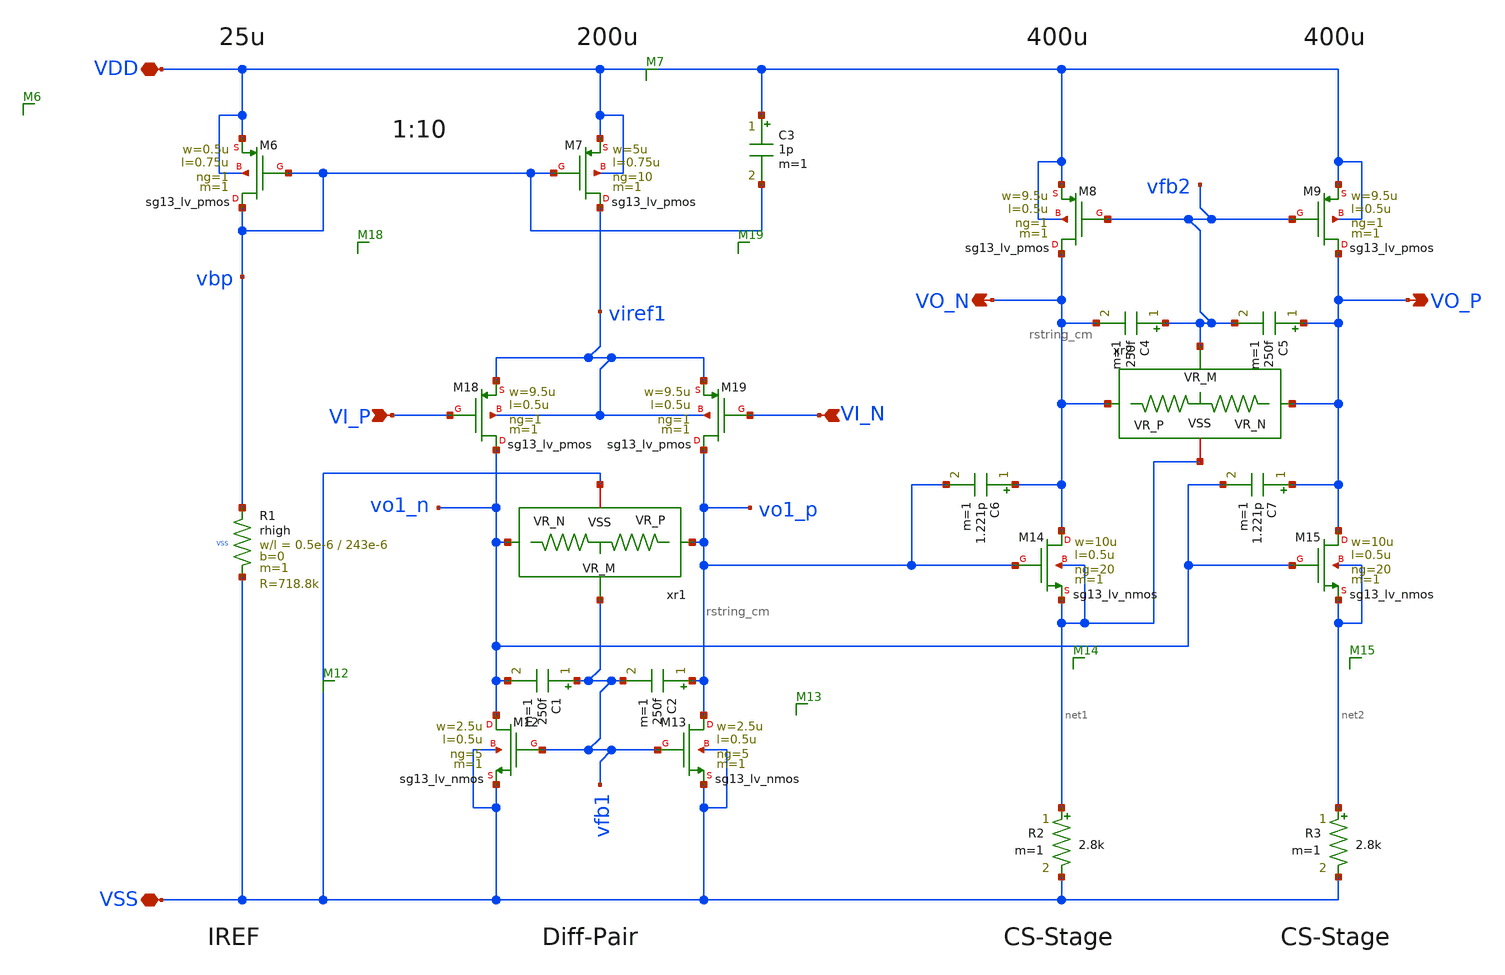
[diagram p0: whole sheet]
** sch_path: macros/filter_cmos5l/schematic/xschem/amp_no_enable.sch
**.subckt amp_no_enable VSS VDD VI_P VI_N VO_P VO_N
*.iopin VSS
*.iopin VDD
*.ipin VI_P
*.ipin VI_N
*.opin VO_P
*.opin VO_N
xr1 vfb1 vo1_n vo1_p VSS rstring_cm
xr2 vfb2 VO_P VO_N net1 rstring_cm
XM6 vbp vbp VDD VDD sg13_lv_pmos w=0.5u l=0.75u ng=1 m=1 mm_ok=1
XM7 viref1 vbp VDD VDD sg13_lv_pmos w=5u l=0.75u ng=10 m=1 mm_ok=1
XM8 VO_N vfb2 VDD VDD sg13_lv_pmos w=9.5u l=0.5u ng=1 m=1 mm_ok=1
XM9 VO_P vfb2 VDD VDD sg13_lv_pmos w=9.5u l=0.5u ng=1 m=1 mm_ok=1
XM12 vo1_n vfb1 VSS VSS sg13_lv_nmos w=2.5u l=0.5u ng=5 m=1 mm_ok=1
XM13 vo1_p vfb1 VSS VSS sg13_lv_nmos w=2.5u l=0.5u ng=5 m=1 mm_ok=1
XM14 VO_N vo1_p net1 net1 sg13_lv_nmos w=10u l=0.5u ng=20 m=1 mm_ok=1
XM15 VO_P vo1_n net2 net2 sg13_lv_nmos w=10u l=0.5u ng=20 m=1 mm_ok=1
XM18 vo1_n VI_P viref1 viref1 sg13_lv_pmos w=9.5u l=0.5u ng=1 m=1 mm_ok=1
XM19 vo1_p VI_N viref1 viref1 sg13_lv_pmos w=9.5u l=0.5u ng=1 m=1 mm_ok=1
XR1 vbp VSS VSS rhigh w=0.5e-6 l=243e-6 m=1 b=0 mm_ok=1
C6 VO_N vo1_p 1.221p m=1
C1 vfb1 vo1_n 250f m=1
C7 VO_P vo1_n 1.221p m=1
C3 VDD vbp 1p m=1
C2 vo1_p vfb1 250f m=1
C4 vfb2 VO_N 250f m=1
C5 VO_P vfb2 250f m=1
R2 net1 VSS 2.8k m=1
R3 net2 VSS 2.8k m=1
**.ends

* expanding   symbol:  rstring_cm.sym # of pins=4
** sym_path: rstring_cm.sym
** sch_path: rstring_cm.sch
.subckt rstring_cm VR_M VR_N VR_P VSS
*.iopin VSS
*.ipin VR_P
*.ipin VR_N
*.opin VR_M
R1 VR_P VR_M 1Meg m=1
R4 VR_M VR_N 1Meg m=1
.ends

.end
